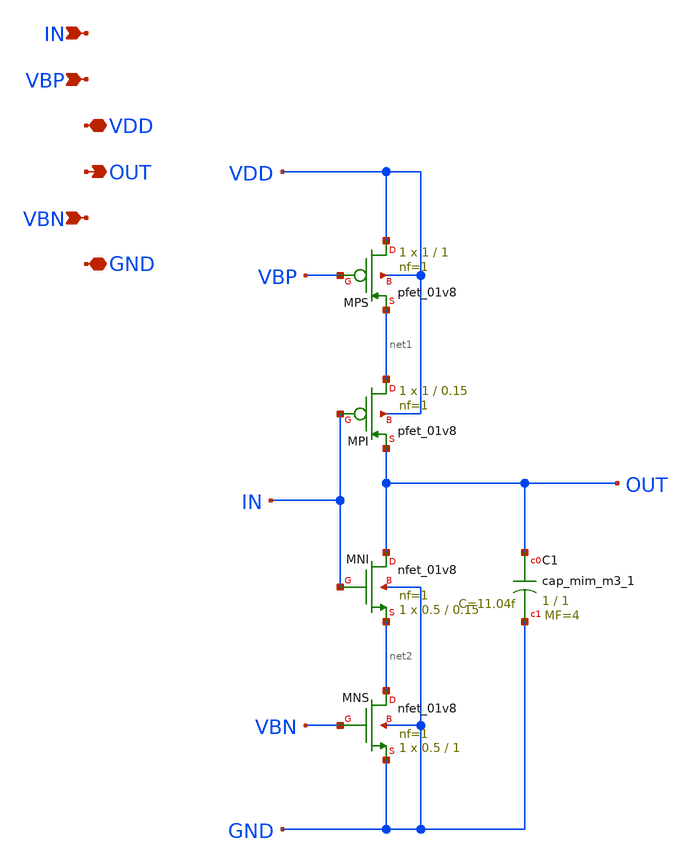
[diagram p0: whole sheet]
** sch_path: blocks/06_Clock_gen/xschem/B6_DELAY_CS.sch
**.subckt B6_DELAY_CS IN VBP VDD OUT VBN GND
*.ipin IN
*.ipin VBP
*.iopin VDD
*.opin OUT
*.ipin VBN
*.iopin GND
XMPS VDD VBP net1 VDD sky130_fd_pr__pfet_01v8 L=1 W=1 nf=1 ad='int((1 + 1)/2) * 1 / 1 * 0.29' as='int((1 + 2)/2) * 1 / 1 * 0.29'
+ pd='2*int((1 + 1)/2) * (1 / 1 + 0.29)' ps='2*int((1 + 2)/2) * (1 / 1 + 0.29)' nrd='0.29 / 1 ' nrs='0.29 / 1 '
+ sa=0 sb=0 sd=0 mult=1 m=1
XMPI net1 IN OUT VDD sky130_fd_pr__pfet_01v8 L=0.15 W=1 nf=1 ad='int((1 + 1)/2) * 1 / 1 * 0.29' as='int((1 + 2)/2) * 1 / 1 * 0.29'
+ pd='2*int((1 + 1)/2) * (1 / 1 + 0.29)' ps='2*int((1 + 2)/2) * (1 / 1 + 0.29)' nrd='0.29 / 1 ' nrs='0.29 / 1 '
+ sa=0 sb=0 sd=0 mult=1 m=1
XMNI OUT IN net2 GND sky130_fd_pr__nfet_01v8 L=0.15 W=0.5 nf=1 ad='int((1 + 1)/2) * 0.5 / 1 * 0.29' as='int((1 + 2)/2) * 0.5 / 1 * 0.29'
+ pd='2*int((1 + 1)/2) * (0.5 / 1 + 0.29)' ps='2*int((1 + 2)/2) * (0.5 / 1 + 0.29)' nrd='0.29 / 0.5 ' nrs='0.29 / 0.5 '
+ sa=0 sb=0 sd=0 mult=1 m=1
XMNS net2 VBN GND GND sky130_fd_pr__nfet_01v8 L=1 W=0.5 nf=1 ad='int((1 + 1)/2) * 0.5 / 1 * 0.29' as='int((1 + 2)/2) * 0.5 / 1 * 0.29'
+ pd='2*int((1 + 1)/2) * (0.5 / 1 + 0.29)' ps='2*int((1 + 2)/2) * (0.5 / 1 + 0.29)' nrd='0.29 / 0.5 ' nrs='0.29 / 0.5 '
+ sa=0 sb=0 sd=0 mult=1 m=1
XC1 OUT GND sky130_fd_pr__cap_mim_m3_1 W=1 L=1 MF=4 m=4
**.ends
.end
